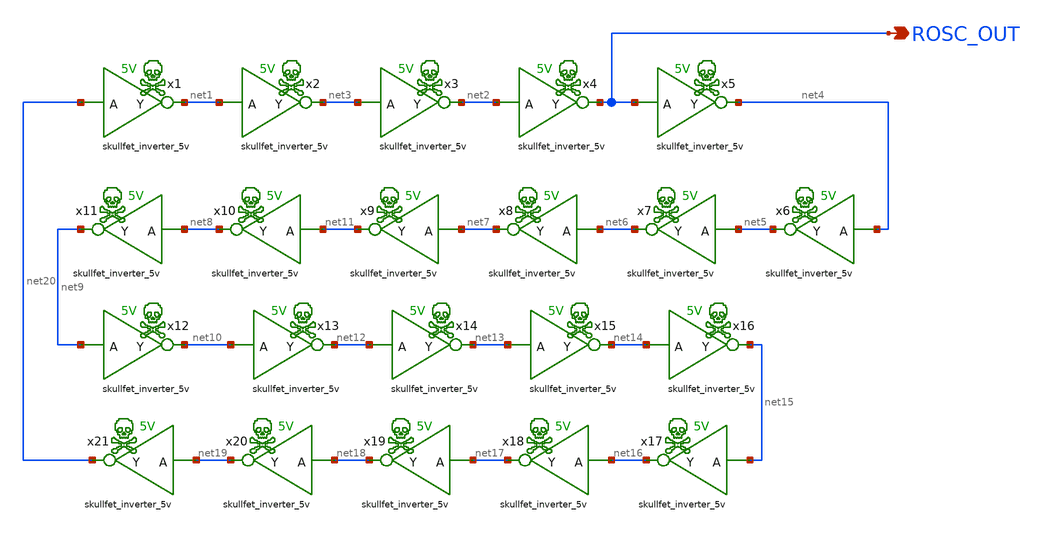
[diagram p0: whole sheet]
** sch_path: xschem/ring.sch
**.subckt ring ROSC_OUT
*.opin ROSC_OUT
x1 net20 net1 skullfet_inverter_5v
x2 net1 net3 skullfet_inverter_5v
x3 net3 net2 skullfet_inverter_5v
x4 net2 ROSC_OUT skullfet_inverter_5v
x5 ROSC_OUT net4 skullfet_inverter_5v
x7 net5 net6 skullfet_inverter_5v
x6 net4 net5 skullfet_inverter_5v
x8 net6 net7 skullfet_inverter_5v
x9 net7 net11 skullfet_inverter_5v
x10 net11 net8 skullfet_inverter_5v
x11 net8 net9 skullfet_inverter_5v
x12 net9 net10 skullfet_inverter_5v
x13 net10 net12 skullfet_inverter_5v
x14 net12 net13 skullfet_inverter_5v
x15 net13 net14 skullfet_inverter_5v
x16 net14 net15 skullfet_inverter_5v
x17 net15 net16 skullfet_inverter_5v
x18 net16 net17 skullfet_inverter_5v
x19 net17 net18 skullfet_inverter_5v
x20 net18 net19 skullfet_inverter_5v
x21 net19 net20 skullfet_inverter_5v
**.ends

* expanding   symbol:  skullfet_inverter_5v.sym # of pins=2
** sym_path: xschem/skullfet_inverter_5v.sym
** sch_path: xschem/skullfet_inverter_5v.sch
.subckt skullfet_inverter_5v A Y
*.ipin A
*.opin Y
x1 A Y VAPWR skullfet_inverter_5v_pwr
.ends


* expanding   symbol:  skullfet_inverter_5v_pwr.sym # of pins=3
** sym_path: xschem/skullfet_inverter_5v_pwr.sym
** sch_path: xschem/skullfet_inverter_5v_pwr.sch
.subckt skullfet_inverter_5v_pwr A Y VDD
*.ipin A
*.opin Y
*.ipin VDD
XM1 Y A VDD VDD sky130_fd_pr__pfet_g5v0d10v5 L=0.5 W=4.5 nf=1 ad=5.3775 as=7.5825 pd=12.07 ps=29.53 nrd='0.29 / 4.5 '
+ nrs='0.29 / 4.5 ' sa=0 sb=0 sd=0 mult=1 m=1
XM2 Y A VGND VGND sky130_fd_pr__nfet_g5v0d10v5 L=0.5 W=4.5 nf=1 ad=7.8525 as=5.1075 pd=29.65 ps=11.95
+ nrd='0.29 / 4.5 ' nrs='0.29 / 4.5 ' sa=0 sb=0 sd=0 mult=1 m=1
.ends

.GLOBAL VAPWR
.GLOBAL VGND
.end
